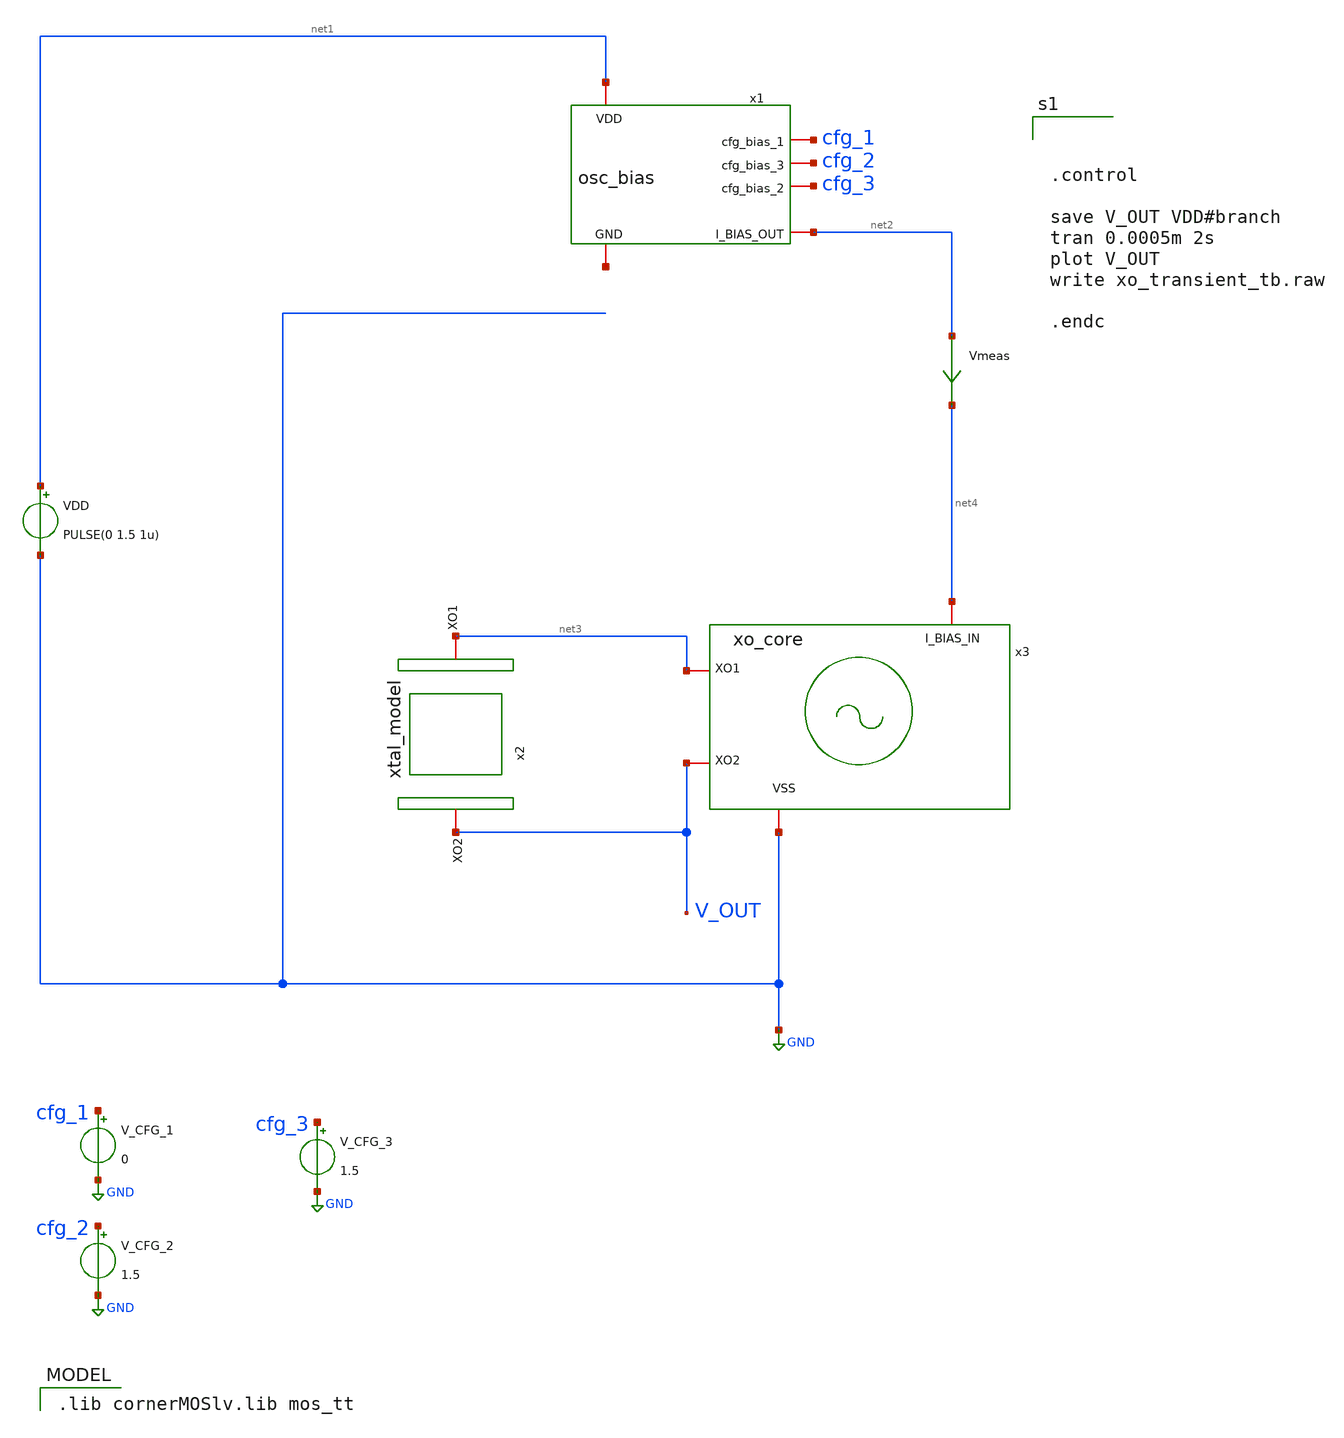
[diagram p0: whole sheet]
** sch_path: xo_transient_tb.sch
**.subckt xo_transient_tb
VDD net1 GND PULSE(0 1.5 1u)
x1 net1 cfg_1 cfg_2 cfg_3 net5 net2 osc_bias
x2 net3 V_OUT xtal_model
x3 net4 V_OUT net3 GND xo_core
V_CFG_1 cfg_1 GND 0
V_CFG_2 cfg_2 GND 1.5
V_CFG_3 cfg_3 GND 1.5
Vmeas net2 net4 0
.save i(vmeas)
**** begin user architecture code



.control

save V_OUT VDD#branch
tran 0.0005m 2s
plot V_OUT
write xo_transient_tb.raw

.endc


 .lib cornerMOSlv.lib mos_tt

**** end user architecture code
**.ends

* expanding   symbol:  osc_bias.sym # of pins=6
** sym_path: osc_bias.sym
** sch_path: osc_bias.sch
.subckt osc_bias VDD cfg_bias_1 cfg_bias_3 cfg_bias_2 GND I_BIAS_OUT
*.iopin VDD
*.iopin GND
*.iopin I_BIAS_OUT
*.iopin cfg_bias_1
*.iopin cfg_bias_2
*.iopin cfg_bias_3
XM1 vp_bias vp_bias VDD VDD sg13_lv_pmos w=1u l=10u ng=1 m=1 mm_ok=1
XM3 vp_bias vp_bias net2 net1 sg13_lv_nmos w=0.25u l=10u ng=1 m=1 mm_ok=1
XM4 net2 net2 net3 net1 sg13_lv_nmos w=0.25u l=10u ng=1 m=1 mm_ok=1
XM5 net3 net3 net1 net1 sg13_lv_nmos w=0.25u l=10u ng=1 m=1 mm_ok=1
XM2 net7 vp_bias VDD VDD sg13_lv_pmos w=0.5u l=10u ng=1 m=1 mm_ok=1
XM6 I_BIAS_OUT cfg_bias_1 net7 VDD sg13_lv_pmos w=0.5u l=5u ng=1 m=1 mm_ok=1
XM7 net4 vp_bias VDD VDD sg13_lv_pmos w=0.5u l=10u ng=1 m=1 mm_ok=1
XM8 net5 vp_bias VDD VDD sg13_lv_pmos w=0.5u l=10u ng=1 m=1 mm_ok=1
XM9 I_BIAS_OUT cfg_bias_2 net4 VDD sg13_lv_pmos w=0.5u l=10u ng=1 m=1 mm_ok=1
XM10 I_BIAS_OUT cfg_bias_3 net5 VDD sg13_lv_pmos w=0.5u l=10u ng=1 m=1 mm_ok=1
XM11 net1 net1 net6 net1 sg13_lv_nmos w=0.25u l=10u ng=1 m=1 mm_ok=1
Vmeas net6 GND 0
.save i(vmeas)
.ends


* expanding   symbol:  xtal_model.sym # of pins=2
** sym_path: xtal_model.sym
** sch_path: xtal_model.sch
.subckt xtal_model XO1 XO2
*.iopin XO2
*.iopin XO1
R1 XO1 net1 1k m=1
Cm net1 net2 1p m=1
C0 XO1 XO2 1p m=1
Lm net2 XO2 1n m=1
.ends


* expanding   symbol:  xo_core.sym # of pins=4
** sym_path: xo_core.sym
** sch_path: xo_core.sch
.subckt xo_core I_BIAS_IN XO2 XO1 VSS
*.iopin VSS
*.ipin I_BIAS_IN
*.iopin XO1
*.iopin XO2
XM2 net1 XO1 XO1 XO1 sg13_lv_pmos w=2u l=2u ng=1 m=1 mm_ok=1
XM3 XO2 net1 net1 net1 sg13_lv_pmos w=2u l=2u ng=1 m=1 mm_ok=1
XM1 XO2 XO1 VSS VSS sg13_lv_nmos w=1.0u l=1.0u ng=1 m=1 mm_ok=1
C2 XO2 VSS 8p m=1
C1 XO1 VSS 8p m=1
Vmeas I_BIAS_IN XO2 0
.save i(vmeas)
.ends

.GLOBAL GND
.end
